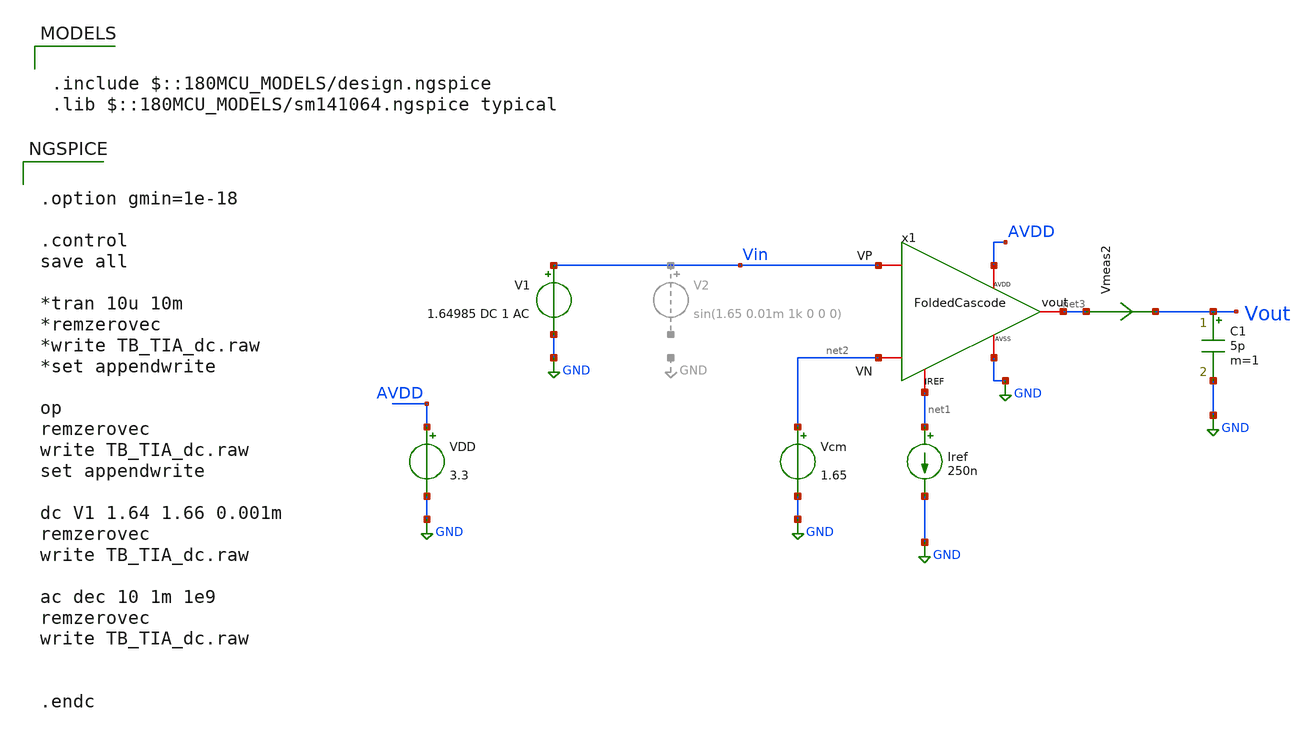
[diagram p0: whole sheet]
** sch_path: Voltage_Reference/LDO/Folded/TB_Folded_dc.sch
**.subckt TB_Folded_dc
VDD AVDD GND 3.3
Iref net1 GND 250n
Vcm net2 GND 1.65
Vmeas2 net3 Vout 0
.save i(vmeas2)
C1 Vout GND 5p m=1
x1 Vin net2 net3 net1 AVDD GND FoldedCascode
V1 Vin GND 1.64985 DC 1 AC
**** begin user architecture code

.include $::180MCU_MODELS/design.ngspice
.lib $::180MCU_MODELS/sm141064.ngspice typical



.option gmin=1e-18

.control
save all

*tran 10u 10m
*remzerovec
*write TB_TIA_dc.raw
*set appendwrite

op
remzerovec
write TB_TIA_dc.raw
set appendwrite

dc V1 1.64 1.66 0.001m
remzerovec
write TB_TIA_dc.raw

ac dec 10 1m 1e9
remzerovec
write TB_TIA_dc.raw


.endc


**** end user architecture code
**.ends
.GLOBAL GND
.end
